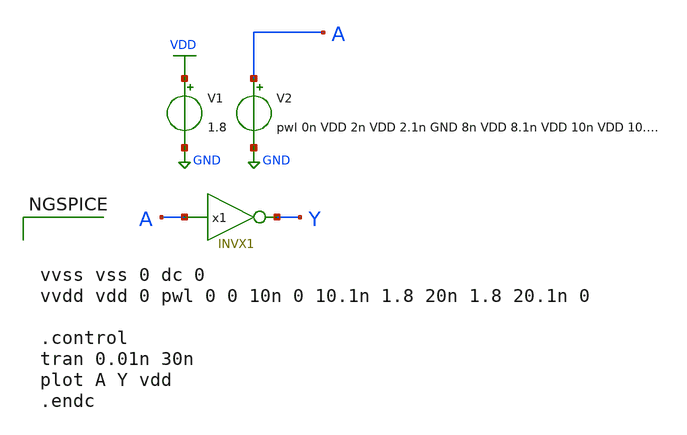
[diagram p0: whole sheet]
** sch_path: sky130A/libs.tech/xschem/sky130_tests/test_INVX1.sch
**.subckt test_INVX1
V2 A GND pwl 0n VDD 2n VDD 2.1n GND 8n VDD 8.1n VDD 10n VDD 10.1n GND 13.9n GND 14n VDD
V1 VDD GND 1.8
x1 A Y INVX1 VDD VSS INVX1
**** begin user architecture code

.lib $::SKYWATER_MODELS/sky130.lib.spice tt


**** end user architecture code
**.ends

* expanding   symbol:  sky130_tests/INVX1.sym # of pins=2
** sym_path: sky130A/libs.tech/xschem/sky130_tests/INVX1.sym
** sch_path: sky130A/libs.tech/xschem/sky130_tests/INVX1.sch
.subckt INVX1 A Y
*.ipin A
*.opin Y
XM1 Y A VSSPIN VSSPIN sky130_fd_pr__nfet_01v8 L=0.15 W=3 nf=1 ad='int((nf+1)/2) * W/nf * 0.29' as='int((nf+2)/2) * W/nf * 0.29'
+ pd='2*int((nf+1)/2) * (W/nf + 0.29)' ps='2*int((nf+2)/2) * (W/nf + 0.29)' nrd='0.29 / W' nrs='0.29 / W'
+ sa=0 sb=0 sd=0 mult=1 m=1
XM2 Y A VDDPIN VDDPIN sky130_fd_pr__pfet_01v8 L=0.15 W=2 nf=1 ad='int((nf+1)/2) * W/nf * 0.29' as='int((nf+2)/2) * W/nf * 0.29'
+ pd='2*int((nf+1)/2) * (W/nf + 0.29)' ps='2*int((nf+2)/2) * (W/nf + 0.29)' nrd='0.29 / W' nrs='0.29 / W'
+ sa=0 sb=0 sd=0 mult=1 m=1
XM3 Y A VDDPIN VDDPIN sky130_fd_pr__pfet_01v8 L=0.15 W=2 nf=1 ad='int((nf+1)/2) * W/nf * 0.29' as='int((nf+2)/2) * W/nf * 0.29'
+ pd='2*int((nf+1)/2) * (W/nf + 0.29)' ps='2*int((nf+2)/2) * (W/nf + 0.29)' nrd='0.29 / W' nrs='0.29 / W'
+ sa=0 sb=0 sd=0 mult=1 m=1
.ends

.GLOBAL GND
.GLOBAL VDD
**** begin user architecture code



vvss vss 0 dc 0
vvdd vdd 0 pwl 0 0 10n 0 10.1n 1.8 20n 1.8 20.1n 0

.control
tran 0.01n 30n
plot A Y vdd
.endc


**** end user architecture code
.end
